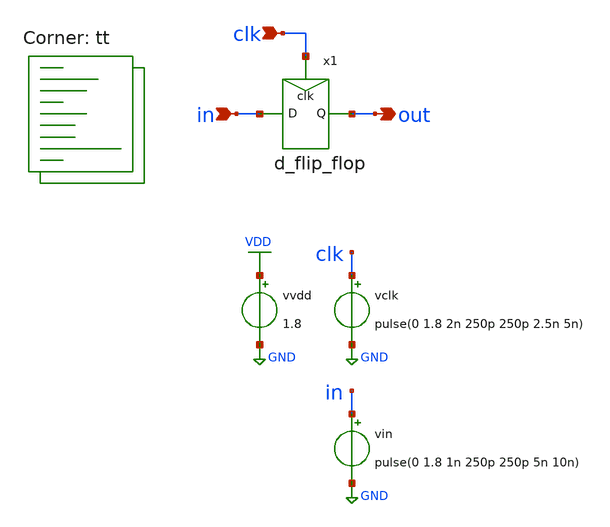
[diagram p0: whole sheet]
** sch_path: xschem/sim/tb_d_flip_flop.sch
**.subckt tb_d_flip_flop out in clk
*.opin out
*.ipin in
*.ipin clk
vvdd VDD GND 1.8
vclk clk GND pulse(0 1.8 2n 250p 250p 2.5n 5n)
x1 clk out in d_flip_flop
vin in GND pulse(0 1.8 1n 250p 250p 5n 10n)
**** begin user architecture code
.lib $::SKYWATER_MODELS/sky130.lib.spice tt


.control
* Transient analysis
TRAN 1p 20n
save all
set filetype=binary
write tb_d_flip_flop_tran.raw
.endc


**** end user architecture code
**.ends

* expanding   symbol:  d_flip_flop.sym # of pins=3
** sym_path: xschem/d_flip_flop.sym
** sch_path: xschem/d_flip_flop.sch
.subckt d_flip_flop clk Q D
*.ipin clk
*.ipin D
*.opin Q
XM1 clk_b clk GND GND sky130_fd_pr__nfet_01v8 L=0.15 W=0.84 nf=1 ad='int((nf+1)/2) * W/nf * 0.29' as='int((nf+2)/2) * W/nf * 0.29'
+ pd='2*int((nf+1)/2) * (W/nf + 0.29)' ps='2*int((nf+2)/2) * (W/nf + 0.29)' nrd='0.29 / W' nrs='0.29 / W'
+ sa=0 sb=0 sd=0 mult=1 m=1
XM2 clk_b clk VDD VDD sky130_fd_pr__pfet_01v8 L=0.15 W=1.68 nf=1 ad='int((nf+1)/2) * W/nf * 0.29' as='int((nf+2)/2) * W/nf * 0.29'
+ pd='2*int((nf+1)/2) * (W/nf + 0.29)' ps='2*int((nf+2)/2) * (W/nf + 0.29)' nrd='0.29 / W' nrs='0.29 / W'
+ sa=0 sb=0 sd=0 mult=1 m=1
XM3 net1 clk net6 VDD sky130_fd_pr__pfet_01v8 L=0.15 W=0.42 nf=1 ad='int((nf+1)/2) * W/nf * 0.29' as='int((nf+2)/2) * W/nf * 0.29'
+ pd='2*int((nf+1)/2) * (W/nf + 0.29)' ps='2*int((nf+2)/2) * (W/nf + 0.29)' nrd='0.29 / W' nrs='0.29 / W'
+ sa=0 sb=0 sd=0 mult=1 m=1
XM4 net6 D VDD VDD sky130_fd_pr__pfet_01v8 L=0.15 W=0.42 nf=1 ad='int((nf+1)/2) * W/nf * 0.29' as='int((nf+2)/2) * W/nf * 0.29'
+ pd='2*int((nf+1)/2) * (W/nf + 0.29)' ps='2*int((nf+2)/2) * (W/nf + 0.29)' nrd='0.29 / W' nrs='0.29 / W'
+ sa=0 sb=0 sd=0 mult=1 m=1
XM5 net1 clk_b net5 GND sky130_fd_pr__nfet_01v8 L=0.15 W=0.42 nf=1 ad='int((nf+1)/2) * W/nf * 0.29' as='int((nf+2)/2) * W/nf * 0.29'
+ pd='2*int((nf+1)/2) * (W/nf + 0.29)' ps='2*int((nf+2)/2) * (W/nf + 0.29)' nrd='0.29 / W' nrs='0.29 / W'
+ sa=0 sb=0 sd=0 mult=1 m=1
XM6 net5 D GND GND sky130_fd_pr__nfet_01v8 L=0.15 W=0.42 nf=1 ad='int((nf+1)/2) * W/nf * 0.29' as='int((nf+2)/2) * W/nf * 0.29'
+ pd='2*int((nf+1)/2) * (W/nf + 0.29)' ps='2*int((nf+2)/2) * (W/nf + 0.29)' nrd='0.29 / W' nrs='0.29 / W'
+ sa=0 sb=0 sd=0 mult=1 m=1
XM7 net2 net1 VDD VDD sky130_fd_pr__pfet_01v8 L=0.15 W=0.42 nf=1 ad='int((nf+1)/2) * W/nf * 0.29' as='int((nf+2)/2) * W/nf * 0.29'
+ pd='2*int((nf+1)/2) * (W/nf + 0.29)' ps='2*int((nf+2)/2) * (W/nf + 0.29)' nrd='0.29 / W' nrs='0.29 / W'
+ sa=0 sb=0 sd=0 mult=1 m=1
XM8 net2 net1 GND GND sky130_fd_pr__nfet_01v8 L=0.15 W=0.42 nf=1 ad='int((nf+1)/2) * W/nf * 0.29' as='int((nf+2)/2) * W/nf * 0.29'
+ pd='2*int((nf+1)/2) * (W/nf + 0.29)' ps='2*int((nf+2)/2) * (W/nf + 0.29)' nrd='0.29 / W' nrs='0.29 / W'
+ sa=0 sb=0 sd=0 mult=1 m=1
XM9 net1 clk_b net4 VDD sky130_fd_pr__pfet_01v8 L=0.15 W=0.42 nf=1 ad='int((nf+1)/2) * W/nf * 0.29' as='int((nf+2)/2) * W/nf * 0.29'
+ pd='2*int((nf+1)/2) * (W/nf + 0.29)' ps='2*int((nf+2)/2) * (W/nf + 0.29)' nrd='0.29 / W' nrs='0.29 / W'
+ sa=0 sb=0 sd=0 mult=1 m=1
XM10 net4 net2 VDD VDD sky130_fd_pr__pfet_01v8 L=0.15 W=0.42 nf=1 ad='int((nf+1)/2) * W/nf * 0.29' as='int((nf+2)/2) * W/nf * 0.29'
+ pd='2*int((nf+1)/2) * (W/nf + 0.29)' ps='2*int((nf+2)/2) * (W/nf + 0.29)' nrd='0.29 / W' nrs='0.29 / W'
+ sa=0 sb=0 sd=0 mult=1 m=1
XM11 net1 clk net3 GND sky130_fd_pr__nfet_01v8 L=0.15 W=0.42 nf=1 ad='int((nf+1)/2) * W/nf * 0.29' as='int((nf+2)/2) * W/nf * 0.29'
+ pd='2*int((nf+1)/2) * (W/nf + 0.29)' ps='2*int((nf+2)/2) * (W/nf + 0.29)' nrd='0.29 / W' nrs='0.29 / W'
+ sa=0 sb=0 sd=0 mult=1 m=1
XM12 net3 net2 GND GND sky130_fd_pr__nfet_01v8 L=0.15 W=0.42 nf=1 ad='int((nf+1)/2) * W/nf * 0.29' as='int((nf+2)/2) * W/nf * 0.29'
+ pd='2*int((nf+1)/2) * (W/nf + 0.29)' ps='2*int((nf+2)/2) * (W/nf + 0.29)' nrd='0.29 / W' nrs='0.29 / W'
+ sa=0 sb=0 sd=0 mult=1 m=1
XM13 net7 clk_b net9 VDD sky130_fd_pr__pfet_01v8 L=0.15 W=0.42 nf=1 ad='int((nf+1)/2) * W/nf * 0.29'
+ as='int((nf+2)/2) * W/nf * 0.29' pd='2*int((nf+1)/2) * (W/nf + 0.29)' ps='2*int((nf+2)/2) * (W/nf + 0.29)'
+ nrd='0.29 / W' nrs='0.29 / W' sa=0 sb=0 sd=0 mult=1 m=1
XM14 net9 net2 VDD VDD sky130_fd_pr__pfet_01v8 L=0.15 W=0.42 nf=1 ad='int((nf+1)/2) * W/nf * 0.29' as='int((nf+2)/2) * W/nf * 0.29'
+ pd='2*int((nf+1)/2) * (W/nf + 0.29)' ps='2*int((nf+2)/2) * (W/nf + 0.29)' nrd='0.29 / W' nrs='0.29 / W'
+ sa=0 sb=0 sd=0 mult=1 m=1
XM15 net7 clk net8 GND sky130_fd_pr__nfet_01v8 L=0.15 W=0.42 nf=1 ad='int((nf+1)/2) * W/nf * 0.29' as='int((nf+2)/2) * W/nf * 0.29'
+ pd='2*int((nf+1)/2) * (W/nf + 0.29)' ps='2*int((nf+2)/2) * (W/nf + 0.29)' nrd='0.29 / W' nrs='0.29 / W'
+ sa=0 sb=0 sd=0 mult=1 m=1
XM16 net8 net2 GND GND sky130_fd_pr__nfet_01v8 L=0.15 W=0.42 nf=1 ad='int((nf+1)/2) * W/nf * 0.29' as='int((nf+2)/2) * W/nf * 0.29'
+ pd='2*int((nf+1)/2) * (W/nf + 0.29)' ps='2*int((nf+2)/2) * (W/nf + 0.29)' nrd='0.29 / W' nrs='0.29 / W'
+ sa=0 sb=0 sd=0 mult=1 m=1
XM17 Q net7 VDD VDD sky130_fd_pr__pfet_01v8 L=0.15 W=0.84 nf=1 ad='int((nf+1)/2) * W/nf * 0.29' as='int((nf+2)/2) * W/nf * 0.29'
+ pd='2*int((nf+1)/2) * (W/nf + 0.29)' ps='2*int((nf+2)/2) * (W/nf + 0.29)' nrd='0.29 / W' nrs='0.29 / W'
+ sa=0 sb=0 sd=0 mult=1 m=1
XM18 Q net7 GND GND sky130_fd_pr__nfet_01v8 L=0.15 W=0.42 nf=1 ad='int((nf+1)/2) * W/nf * 0.29' as='int((nf+2)/2) * W/nf * 0.29'
+ pd='2*int((nf+1)/2) * (W/nf + 0.29)' ps='2*int((nf+2)/2) * (W/nf + 0.29)' nrd='0.29 / W' nrs='0.29 / W'
+ sa=0 sb=0 sd=0 mult=1 m=1
XM19 net7 clk net11 VDD sky130_fd_pr__pfet_01v8 L=0.15 W=0.42 nf=1 ad='int((nf+1)/2) * W/nf * 0.29' as='int((nf+2)/2) * W/nf * 0.29'
+ pd='2*int((nf+1)/2) * (W/nf + 0.29)' ps='2*int((nf+2)/2) * (W/nf + 0.29)' nrd='0.29 / W' nrs='0.29 / W'
+ sa=0 sb=0 sd=0 mult=1 m=1
XM20 net11 Q VDD VDD sky130_fd_pr__pfet_01v8 L=0.15 W=0.42 nf=1 ad='int((nf+1)/2) * W/nf * 0.29' as='int((nf+2)/2) * W/nf * 0.29'
+ pd='2*int((nf+1)/2) * (W/nf + 0.29)' ps='2*int((nf+2)/2) * (W/nf + 0.29)' nrd='0.29 / W' nrs='0.29 / W'
+ sa=0 sb=0 sd=0 mult=1 m=1
XM21 net7 clk_b net10 GND sky130_fd_pr__nfet_01v8 L=0.15 W=0.42 nf=1 ad='int((nf+1)/2) * W/nf * 0.29'
+ as='int((nf+2)/2) * W/nf * 0.29' pd='2*int((nf+1)/2) * (W/nf + 0.29)' ps='2*int((nf+2)/2) * (W/nf + 0.29)'
+ nrd='0.29 / W' nrs='0.29 / W' sa=0 sb=0 sd=0 mult=1 m=1
XM22 net10 Q GND GND sky130_fd_pr__nfet_01v8 L=0.15 W=0.42 nf=1 ad='int((nf+1)/2) * W/nf * 0.29' as='int((nf+2)/2) * W/nf * 0.29'
+ pd='2*int((nf+1)/2) * (W/nf + 0.29)' ps='2*int((nf+2)/2) * (W/nf + 0.29)' nrd='0.29 / W' nrs='0.29 / W'
+ sa=0 sb=0 sd=0 mult=1 m=1
.ends

.GLOBAL VDD
.GLOBAL GND
.end
